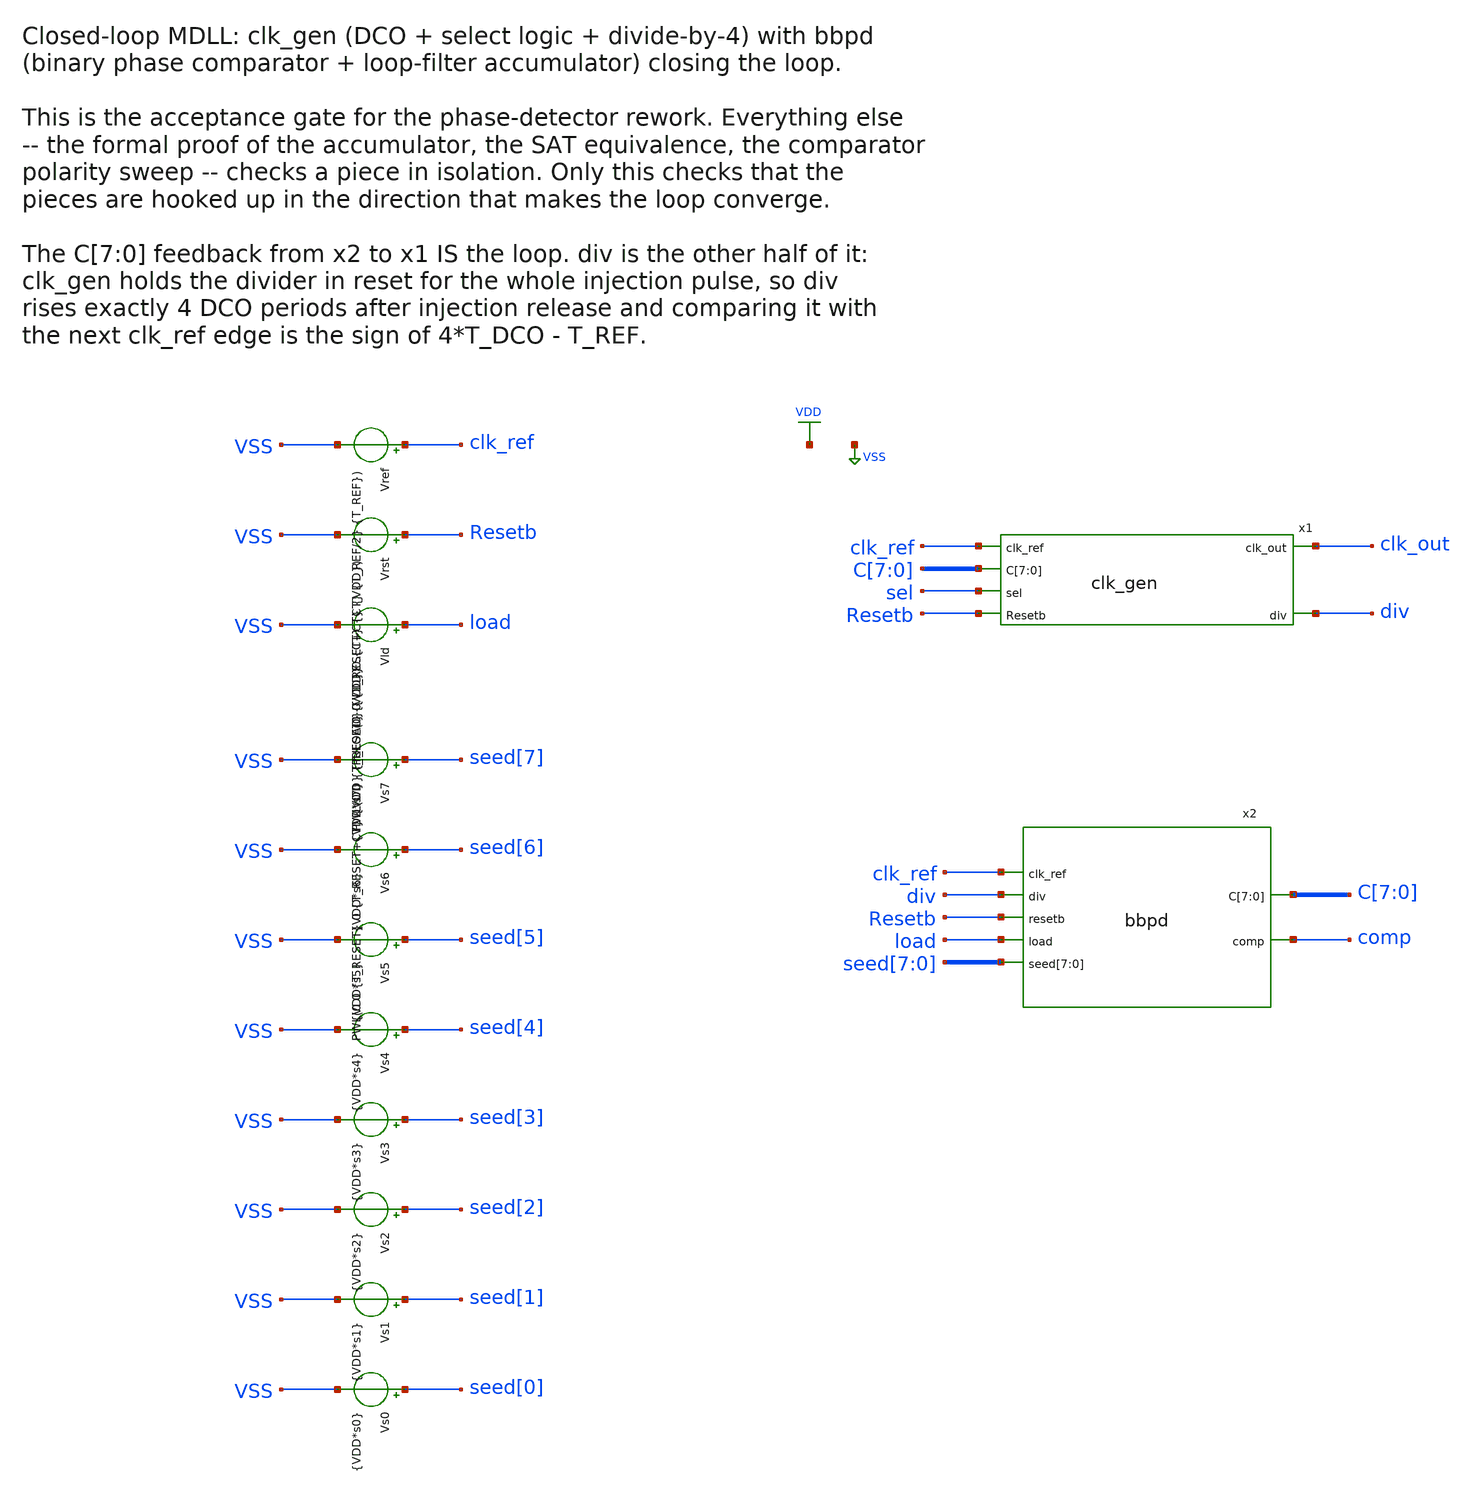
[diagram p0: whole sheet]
** sch_path: TPU5555-main/mdll/mixed_signal_design_blocks/bbpd/test_fine_loop.sch


* This whole block is tcleval()'d: xschem runs it through tcl subst when it
* writes the netlist, so env lookups and command substitutions below are
* expanded. The flip side is that a stray dollar sign or open bracket is a tcl
* error, and a failed tcleval turns the ENTIRE block into a single question
* mark -- silently. That is why the save list, which names the C bus bit by
* bit, lives in the CODE block instead, and why these comments are so careful.
* bbpd/Makefile greps the netlist for that question mark.

* dlf.spice is not a schematic: it is generated from build/01-synth/dlf.v by
* common/sim/gen_rtl_spice.py, which in turn needs yosys to have run. xschem's
* Netlist button knows nothing about that chain, so it is resolved here. rc=0 is
* success; on rc=1 read bbpd/build/mk_dlf.log and expect a stale dlf.spice below.
* mk dlf.spice rc=[file mkdir $env(MSDB_ROOT)/bbpd/build][catch {exec make -s -C $env(MSDB_ROOT)/bbpd simulations/dlf.spice >& $env(MSDB_ROOT)/bbpd/build/mk_dlf.log}]

.LIB cornerMOSlv.lib mos_tt
.OPTIONS KLU
.INCLUDE sg13g2_stdcell.spice
.INCLUDE custom_stdcell.spice

* Absolute, assembled from MSDB_ROOT (exported by tools/xschem) when the netlist
* is written -- the .sch stores the expression, not the path, so the checkout
* stays portable. A relative include cannot work here because the two ways of
* running this deck have different working directories: make runs ngspice from
* bbpd/, while xschem's Simulate button runs it from netlist_dir, which xschemrc
* derives from the working directory -- and the wrapper makes that the REPO ROOT.
.INCLUDE $env(MSDB_ROOT)/clk_gen/simulations/dco_decode.spice
.INCLUDE $env(MSDB_ROOT)/bbpd/simulations/dlf.spice

* Same reason for the raw file, and the same restriction on brackets -- so the
* path is handed to the CODE block as an ngspice variable. setcs, not set: set
* lower-cases its value, and the repo path has capitals in it.
.control
  setcs rawfile = $env(MSDB_ROOT)/bbpd/simulations/test_fine_loop.raw
.endc
.PARAM VDD=1.2
.PARAM T_REF=10n
.PARAM CT=50p
.PARAM T_RESET=1n
.PARAM T_LOAD=T_REF+2n
* Seeded on the FAST side of lock (DCO code 15; lock is 18..19 at tt). A
* ring clearly late -- div missing, or past T_REF/2 -- reads as early in pd
* and walks the code the wrong way; in the MDLL lock_ctrl restarts acquisition
* then (missed injections, code at a rail). bbpd alone has no such guard.
.PARAM SEED=60
.TEMP 27

* SEED bit by bit, for the Vs7..Vs0 sources. ngspice has no bitwise operators
* in .param, so each bit is int(SEED/2^k) - 2*int(SEED/2^(k+1)). These live in
* the header because xschem emits component instances before the user-code
* block, and the sources reference them.
.param s0={int(SEED/1)-2*int(SEED/2)}
.param s1={int(SEED/2)-2*int(SEED/4)}
.param s2={int(SEED/4)-2*int(SEED/8)}
.param s3={int(SEED/8)-2*int(SEED/16)}
.param s4={int(SEED/16)-2*int(SEED/32)}
.param s5={int(SEED/32)-2*int(SEED/64)}
.param s6={int(SEED/64)-2*int(SEED/128)}
.param s7={int(SEED/128)-2*int(SEED/256)}


**.subckt test_fine_loop
x1 clk_ref C[7] C[6] C[5] C[4] C[3] C[2] C[1] C[0] clk_out sel Resetb div clk_gen
Vref clk_ref VSS PULSE(0 {VDD} 0 {CT} {CT} {T_REF/2} {T_REF})
Vrst Resetb VSS PWL(0 0 {T_RESET} 0 {T_RESET+CT} {VDD})
Vld load VSS PWL(0 0 {T_RESET} 0 {T_RESET+CT} {VDD} {T_LOAD} {VDD} {T_LOAD+CT} 0)
Vs7 seed[7] VSS {VDD*s7}
Vs6 seed[6] VSS {VDD*s6}
Vs5 seed[5] VSS {VDD*s5}
Vs4 seed[4] VSS {VDD*s4}
Vs3 seed[3] VSS {VDD*s3}
Vs2 seed[2] VSS {VDD*s2}
Vs1 seed[1] VSS {VDD*s1}
Vs0 seed[0] VSS {VDD*s0}
x2 clk_ref div Resetb load seed[7] seed[6] seed[5] seed[4] seed[3] seed[2] seed[1] seed[0] C[7] C[6] C[5] C[4] C[3] C[2] C[1] C[0] comp bbpd
**** begin user architecture code


VVDD VDD 0 DC {VDD}
VVSS VSS 0 0

.control
  set filetype=ascii
  save clk_ref clk_out div sel comp C[7] C[6] C[5] C[4] C[3] C[2] C[1] C[0]
  tran 10p 400n
  * ASCII raw, not wrdata. wrdata cannot take a bracketed node name without
  * quotes, and a quote cannot survive xschem's value=... attribute without
  * escaping -- unescaped it truncates the control block, and the deck then
  * runs the whole transient before losing it. The raw file carries every
  * saved vector under its real name and simulations/check_lock.py reads it
  * directly.
  *
  * rawfile is set by the header block; see the comment there. This block is
  * deliberately NOT tcleval()'d -- the save list above names C[7]..C[0], and tcl
  * would read those brackets as command substitution.
  write $rawfile
  quit
.endc


**** end user architecture code
**.ends
.GLOBAL VDD
.GLOBAL VSS
.end
